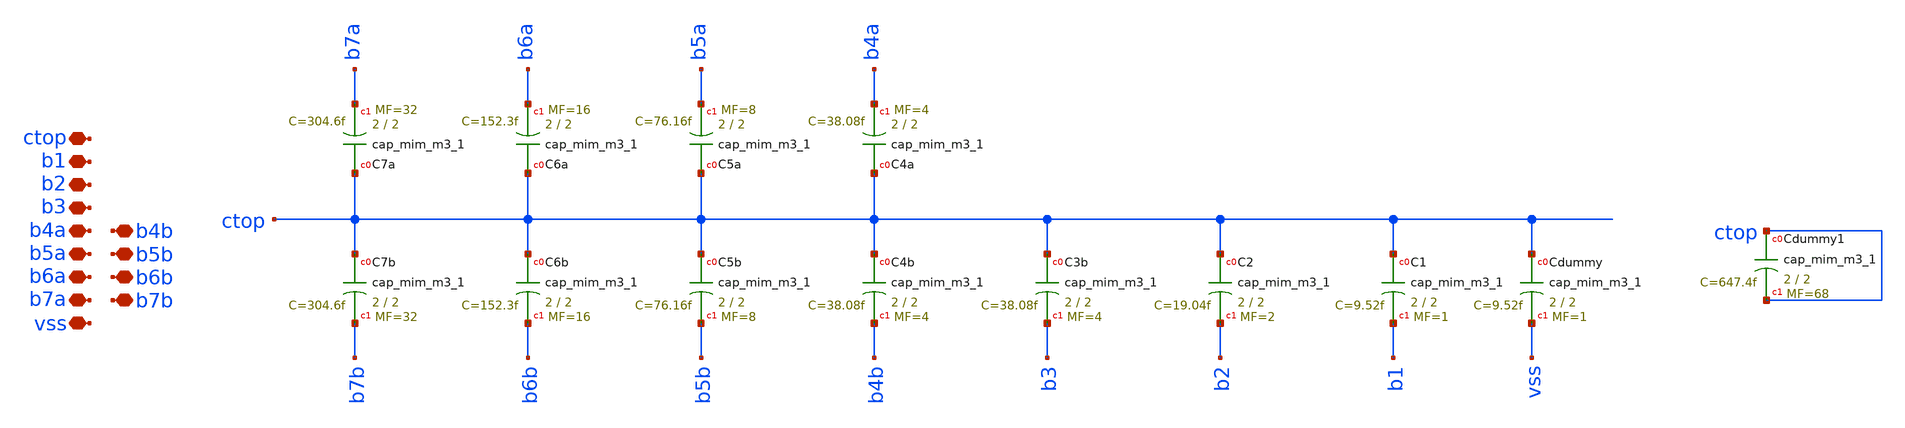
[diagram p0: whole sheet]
** sch_path: xschem/sar-adc/cdac.sch
**.subckt cdac ctop b1 b2 b7a b4a b5a b6a b3 b5b b4b b6b b7b vss
*.iopin ctop
*.iopin b1
*.iopin b2
*.iopin b7a
*.iopin b4a
*.iopin b5a
*.iopin b6a
*.iopin b3
*.iopin b5b
*.iopin b4b
*.iopin b6b
*.iopin b7b
*.iopin vss
XC6b ctop b6b sky130_fd_pr__cap_mim_m3_1 W=2 L=2 MF=16 m=16
XC1 ctop b1 sky130_fd_pr__cap_mim_m3_1 W=2 L=2 MF=1 m=1
XC2 ctop b2 sky130_fd_pr__cap_mim_m3_1 W=2 L=2 MF=2 m=2
XC3b ctop b3 sky130_fd_pr__cap_mim_m3_1 W=2 L=2 MF=4 m=4
XC4b ctop b4b sky130_fd_pr__cap_mim_m3_1 W=2 L=2 MF=4 m=4
XC5b ctop b5b sky130_fd_pr__cap_mim_m3_1 W=2 L=2 MF=8 m=8
XC7b ctop b7b sky130_fd_pr__cap_mim_m3_1 W=2 L=2 MF=32 m=32
XCdummy ctop vss sky130_fd_pr__cap_mim_m3_1 W=2 L=2 MF=1 m=1
XC7a ctop b7a sky130_fd_pr__cap_mim_m3_1 W=2 L=2 MF=32 m=32
XC5a ctop b5a sky130_fd_pr__cap_mim_m3_1 W=2 L=2 MF=8 m=8
XC4a ctop b4a sky130_fd_pr__cap_mim_m3_1 W=2 L=2 MF=4 m=4
XC6a ctop b6a sky130_fd_pr__cap_mim_m3_1 W=2 L=2 MF=16 m=16
XCdummy1 ctop ctop sky130_fd_pr__cap_mim_m3_1 W=2 L=2 MF=68 m=68
**.ends
.end
